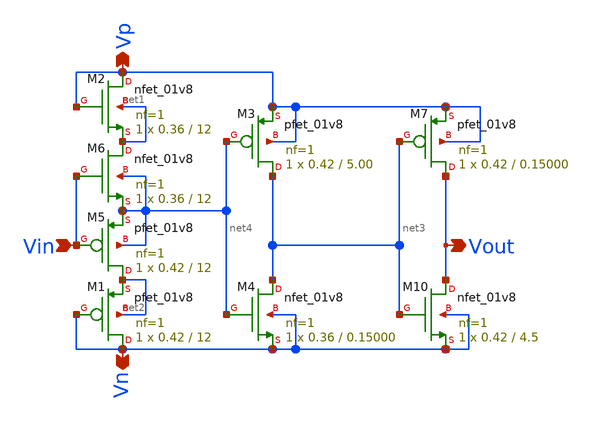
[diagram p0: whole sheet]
** sch_path: xschem/Vth_sch/Symbol/th01.sch
**.subckt th01 Vn Vp Vin Vout
*.opin Vn
*.opin Vp
*.ipin Vin
*.opin Vout
XM1 Vn Vn net2 net2 sky130_fd_pr__pfet_01v8 L=12 W=0.42 nf=1 ad='int((nf+1)/2) * W/nf * 0.29' as='int((nf+2)/2) * W/nf * 0.29'
+ pd='2*int((nf+1)/2) * (W/nf + 0.29)' ps='2*int((nf+2)/2) * (W/nf + 0.29)' nrd='0.29 / W' nrs='0.29 / W'
+ sa=0 sb=0 sd=0 mult=1 m=1
XM2 Vp Vp net1 net1 sky130_fd_pr__nfet_01v8 L=12 W=0.36 nf=1 ad='int((nf+1)/2) * W/nf * 0.29' as='int((nf+2)/2) * W/nf * 0.29'
+ pd='2*int((nf+1)/2) * (W/nf + 0.29)' ps='2*int((nf+2)/2) * (W/nf + 0.29)' nrd='0.29 / W' nrs='0.29 / W'
+ sa=0 sb=0 sd=0 mult=1 m=1
XM7 Vout net3 Vp Vp sky130_fd_pr__pfet_01v8 L=0.15000 W=0.42 nf=1 ad='int((nf+1)/2) * W/nf * 0.29' as='int((nf+2)/2) * W/nf * 0.29'
+ pd='2*int((nf+1)/2) * (W/nf + 0.29)' ps='2*int((nf+2)/2) * (W/nf + 0.29)' nrd='0.29 / W' nrs='0.29 / W'
+ sa=0 sb=0 sd=0 mult=1 m=1
XM10 Vout net3 Vn Vn sky130_fd_pr__nfet_01v8 L=4.5 W=0.42 nf=1 ad='int((nf+1)/2) * W/nf * 0.29' as='int((nf+2)/2) * W/nf * 0.29'
+ pd='2*int((nf+1)/2) * (W/nf + 0.29)' ps='2*int((nf+2)/2) * (W/nf + 0.29)' nrd='0.29 / W' nrs='0.29 / W'
+ sa=0 sb=0 sd=0 mult=1 m=1
XM3 net3 net4 Vp Vp sky130_fd_pr__pfet_01v8 L=5.00 W=0.42 nf=1 ad='int((nf+1)/2) * W/nf * 0.29' as='int((nf+2)/2) * W/nf * 0.29'
+ pd='2*int((nf+1)/2) * (W/nf + 0.29)' ps='2*int((nf+2)/2) * (W/nf + 0.29)' nrd='0.29 / W' nrs='0.29 / W'
+ sa=0 sb=0 sd=0 mult=1 m=1
XM4 net3 net4 Vn Vn sky130_fd_pr__nfet_01v8 L=0.15000 W=0.36 nf=1 ad='int((nf+1)/2) * W/nf * 0.29' as='int((nf+2)/2) * W/nf * 0.29'
+ pd='2*int((nf+1)/2) * (W/nf + 0.29)' ps='2*int((nf+2)/2) * (W/nf + 0.29)' nrd='0.29 / W' nrs='0.29 / W'
+ sa=0 sb=0 sd=0 mult=1 m=1
XM5 net2 Vin net4 net4 sky130_fd_pr__pfet_01v8 L=12 W=0.42 nf=1 ad='int((nf+1)/2) * W/nf * 0.29' as='int((nf+2)/2) * W/nf * 0.29'
+ pd='2*int((nf+1)/2) * (W/nf + 0.29)' ps='2*int((nf+2)/2) * (W/nf + 0.29)' nrd='0.29 / W' nrs='0.29 / W'
+ sa=0 sb=0 sd=0 mult=1 m=1
XM6 net1 Vin net4 net4 sky130_fd_pr__nfet_01v8 L=12 W=0.36 nf=1 ad='int((nf+1)/2) * W/nf * 0.29' as='int((nf+2)/2) * W/nf * 0.29'
+ pd='2*int((nf+1)/2) * (W/nf + 0.29)' ps='2*int((nf+2)/2) * (W/nf + 0.29)' nrd='0.29 / W' nrs='0.29 / W'
+ sa=0 sb=0 sd=0 mult=1 m=1
**.ends
.end
